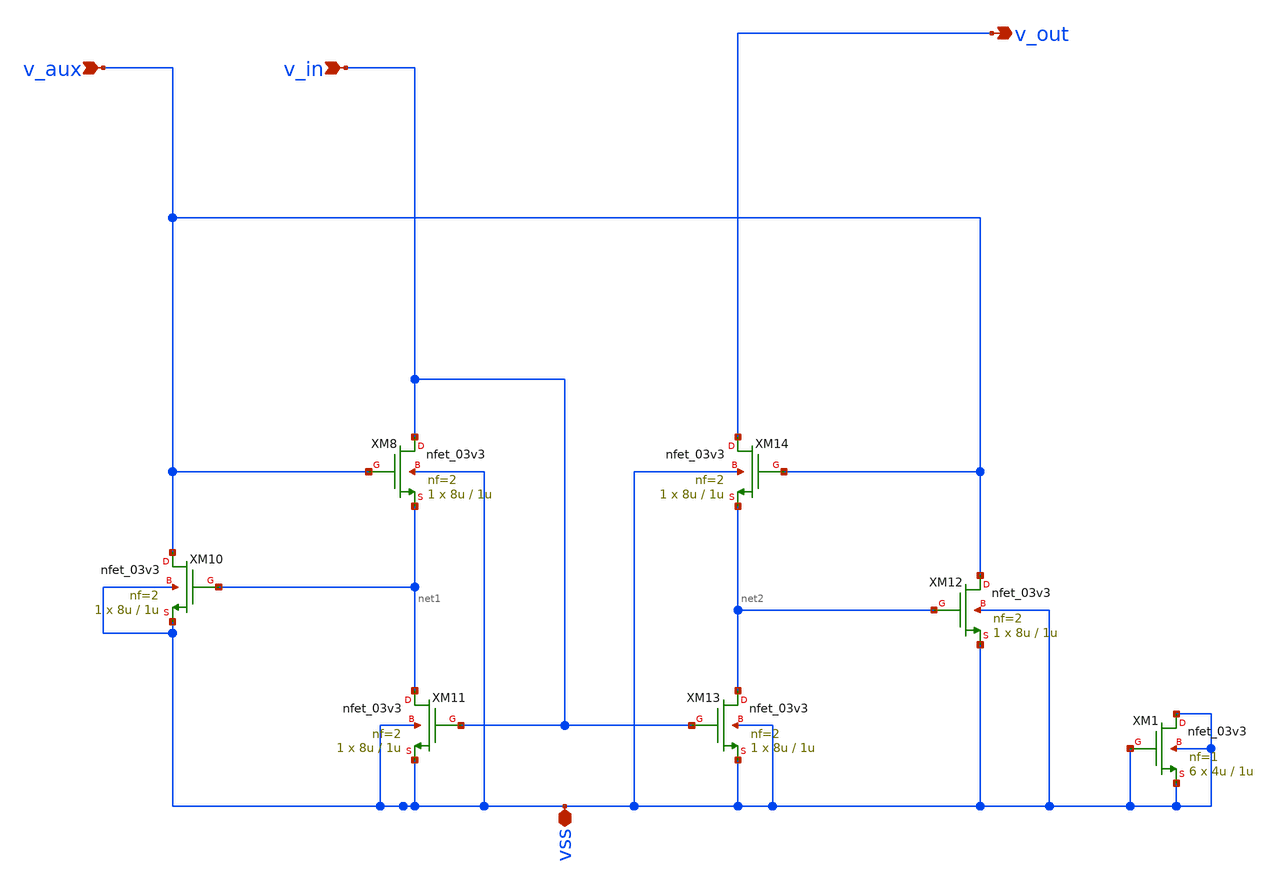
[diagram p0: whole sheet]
** sch_path: blocks/composite/regulated_cascoded_cmirror/A3_core/cascode_cm/cascode_cm.sch
**.subckt cascode_cm v_in vss v_aux v_out
*.ipin v_in
*.iopin vss
*.ipin v_aux
*.opin v_out
XM10 v_aux net1 vss vss nfet_03v3 L=1u W=8u nf=2 ad='int((nf+1)/2) * W/nf * 0.18u' as='int((nf+2)/2) * W/nf * 0.18u'
+ pd='2*int((nf+1)/2) * (W/nf + 0.18u)' ps='2*int((nf+2)/2) * (W/nf + 0.18u)' nrd='0.18u / W' nrs='0.18u / W'
+ sa=0 sb=0 sd=0 m=1
XM8 v_in v_aux net1 vss nfet_03v3 L=1u W=8u nf=2 ad='int((nf+1)/2) * W/nf * 0.18u' as='int((nf+2)/2) * W/nf * 0.18u'
+ pd='2*int((nf+1)/2) * (W/nf + 0.18u)' ps='2*int((nf+2)/2) * (W/nf + 0.18u)' nrd='0.18u / W' nrs='0.18u / W'
+ sa=0 sb=0 sd=0 m=1
XM11 net1 v_in vss vss nfet_03v3 L=1u W=8u nf=2 ad='int((nf+1)/2) * W/nf * 0.18u' as='int((nf+2)/2) * W/nf * 0.18u'
+ pd='2*int((nf+1)/2) * (W/nf + 0.18u)' ps='2*int((nf+2)/2) * (W/nf + 0.18u)' nrd='0.18u / W' nrs='0.18u / W'
+ sa=0 sb=0 sd=0 m=1
XM12 v_aux net2 vss vss nfet_03v3 L=1u W=8u nf=2 ad='int((nf+1)/2) * W/nf * 0.18u' as='int((nf+2)/2) * W/nf * 0.18u'
+ pd='2*int((nf+1)/2) * (W/nf + 0.18u)' ps='2*int((nf+2)/2) * (W/nf + 0.18u)' nrd='0.18u / W' nrs='0.18u / W'
+ sa=0 sb=0 sd=0 m=1
XM13 net2 v_in vss vss nfet_03v3 L=1u W=8u nf=2 ad='int((nf+1)/2) * W/nf * 0.18u' as='int((nf+2)/2) * W/nf * 0.18u'
+ pd='2*int((nf+1)/2) * (W/nf + 0.18u)' ps='2*int((nf+2)/2) * (W/nf + 0.18u)' nrd='0.18u / W' nrs='0.18u / W'
+ sa=0 sb=0 sd=0 m=1
XM14 v_out v_aux net2 vss nfet_03v3 L=1u W=8u nf=2 ad='int((nf+1)/2) * W/nf * 0.18u' as='int((nf+2)/2) * W/nf * 0.18u'
+ pd='2*int((nf+1)/2) * (W/nf + 0.18u)' ps='2*int((nf+2)/2) * (W/nf + 0.18u)' nrd='0.18u / W' nrs='0.18u / W'
+ sa=0 sb=0 sd=0 m=1
XM1 vss vss vss vss nfet_03v3 L=1u W=4u nf=1 ad='int((nf+1)/2) * W/nf * 0.18u' as='int((nf+2)/2) * W/nf * 0.18u'
+ pd='2*int((nf+1)/2) * (W/nf + 0.18u)' ps='2*int((nf+2)/2) * (W/nf + 0.18u)' nrd='0.18u / W' nrs='0.18u / W'
+ sa=0 sb=0 sd=0 m=6
**.ends
.end
